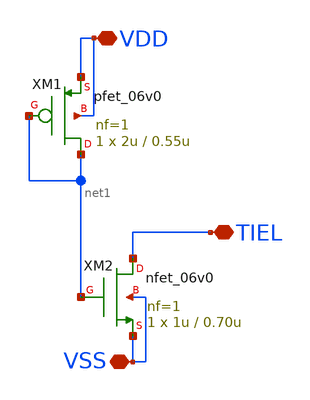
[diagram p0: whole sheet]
** sch_path: designs/libs/core_top/top_io_tie_l/top_io_tie_l.sch
**.subckt top_io_tie_l VSS VDD TIEL
*.iopin VSS
*.iopin VDD
*.iopin TIEL
XM1 net1 net1 VDD VDD pfet_06v0 L=0.55u W=2u nf=1 ad='int((nf+1)/2) * W/nf * 0.18u' as='int((nf+2)/2) * W/nf * 0.18u'
+ pd='2*int((nf+1)/2) * (W/nf + 0.18u)' ps='2*int((nf+2)/2) * (W/nf + 0.18u)' nrd='0.18u / W' nrs='0.18u / W'
+ sa=0 sb=0 sd=0 m=1
XM2 TIEL net1 VSS VSS nfet_06v0 L=0.70u W=1u nf=1 ad='int((nf+1)/2) * W/nf * 0.18u' as='int((nf+2)/2) * W/nf * 0.18u'
+ pd='2*int((nf+1)/2) * (W/nf + 0.18u)' ps='2*int((nf+2)/2) * (W/nf + 0.18u)' nrd='0.18u / W' nrs='0.18u / W'
+ sa=0 sb=0 sd=0 m=1
**.ends
.end
